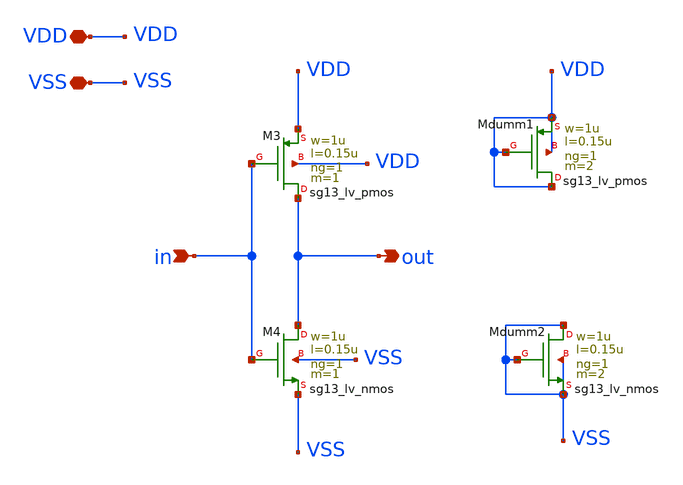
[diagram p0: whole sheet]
** sch_path: xschem/inv_lv.sch
**.subckt inv_lv in out VDD VSS
*.ipin in
*.opin out
*.iopin VDD
*.iopin VSS
XM3 out in VDD VDD sg13_lv_pmos w=1u l=0.15u ng=1 m=1 mm_ok=1
XM4 out in VSS VSS sg13_lv_nmos w=1u l=0.15u ng=1 m=1 mm_ok=1
XMdumm1 VDD VDD VDD VDD sg13_lv_pmos w=1u l=0.15u ng=1 m=2 mm_ok=1
XMdumm2 VSS VSS VSS VSS sg13_lv_nmos w=1u l=0.15u ng=1 m=2 mm_ok=1
**.ends
.end
